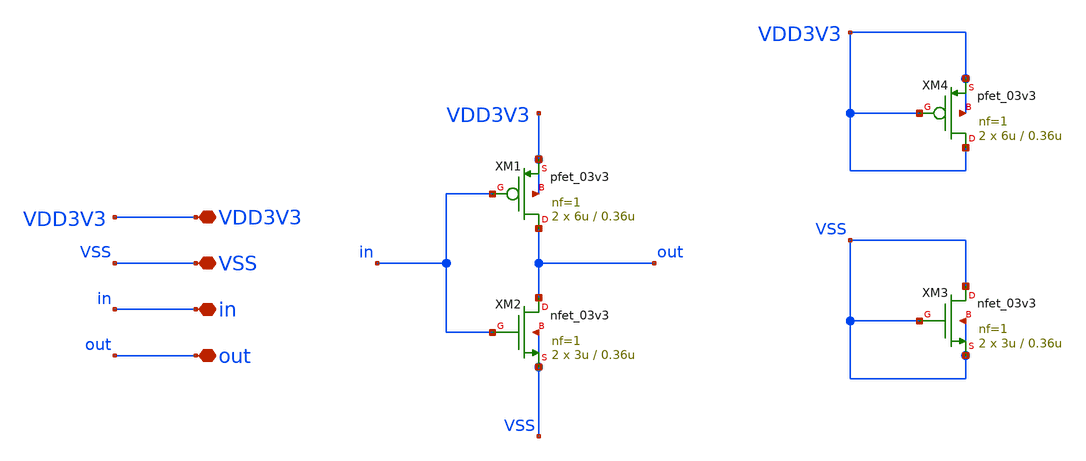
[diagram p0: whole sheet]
** sch_path: designs/libs/core_pga/inverter/inverter.sch
**.subckt inverter VSS VDD3V3 in out
*.iopin VSS
*.iopin VDD3V3
*.iopin in
*.iopin out
XM1 out in VDD3V3 VDD3V3 pfet_03v3 L=0.36u W=6u nf=1 ad='int((nf+1)/2) * W/nf * 0.18u' as='int((nf+2)/2) * W/nf * 0.18u'
+ pd='2*int((nf+1)/2) * (W/nf + 0.18u)' ps='2*int((nf+2)/2) * (W/nf + 0.18u)' nrd='0.18u / W' nrs='0.18u / W'
+ sa=0 sb=0 sd=0 m=2
XM2 out in VSS VSS nfet_03v3 L=0.36u W=3u nf=1 ad='int((nf+1)/2) * W/nf * 0.18u' as='int((nf+2)/2) * W/nf * 0.18u'
+ pd='2*int((nf+1)/2) * (W/nf + 0.18u)' ps='2*int((nf+2)/2) * (W/nf + 0.18u)' nrd='0.18u / W' nrs='0.18u / W'
+ sa=0 sb=0 sd=0 m=2
XM3 VSS VSS VSS VSS nfet_03v3 L=0.36u W=3u nf=1 ad='int((nf+1)/2) * W/nf * 0.18u' as='int((nf+2)/2) * W/nf * 0.18u'
+ pd='2*int((nf+1)/2) * (W/nf + 0.18u)' ps='2*int((nf+2)/2) * (W/nf + 0.18u)' nrd='0.18u / W' nrs='0.18u / W'
+ sa=0 sb=0 sd=0 m=2
XM4 VDD3V3 VDD3V3 VDD3V3 VDD3V3 pfet_03v3 L=0.36u W=6u nf=1 ad='int((nf+1)/2) * W/nf * 0.18u' as='int((nf+2)/2) * W/nf * 0.18u'
+ pd='2*int((nf+1)/2) * (W/nf + 0.18u)' ps='2*int((nf+2)/2) * (W/nf + 0.18u)' nrd='0.18u / W' nrs='0.18u / W'
+ sa=0 sb=0 sd=0 m=2
**.ends
.end
